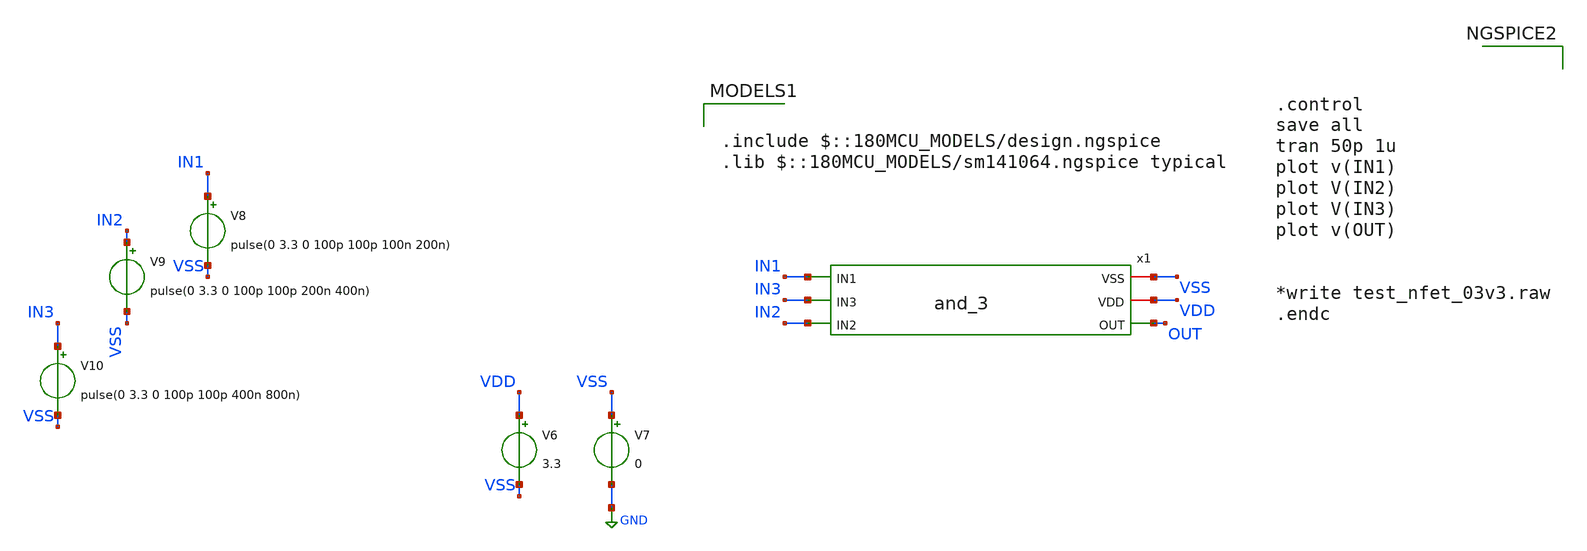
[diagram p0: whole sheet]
** sch_path: Clock_Generator_PAKISTAN_02/Schematics/and_3_TB_ibr.sch
**.subckt and_3_TB_ibr
V6 VDD VSS 3.3
V7 VSS GND 0
V8 IN1 VSS pulse(0 3.3 0 100p 100p 100n 200n)
V9 IN2 VSS pulse(0 3.3 0 100p 100p 200n 400n)
V10 IN3 VSS pulse(0 3.3 0 100p 100p 400n 800n)
x1 IN1 VSS VDD OUT IN3 IN2 and_3
**** begin user architecture code

.include $::180MCU_MODELS/design.ngspice
.lib $::180MCU_MODELS/sm141064.ngspice typical




.control
save all
tran 50p 1u
plot v(IN1)
plot V(IN2)
plot V(IN3)
plot v(OUT)


*write test_nfet_03v3.raw
.endc


**** end user architecture code
**.ends

* expanding   symbol:  and_3.sym # of pins=6
** sym_path: Clock_Generator_PAKISTAN_02/Schematics/and_3.sym
** sch_path: Clock_Generator_PAKISTAN_02/Schematics/and_3.sch
.subckt and_3 IN1 VSS VDD OUT IN3 IN2
*.ipin IN2
*.ipin IN1
*.iopin VSS
*.iopin VDD
*.opin OUT
*.ipin IN3
XM3 net2 IN3 VSS VSS nfet_03v3 L=0.28u W=0.22u nf=1 ad='int((nf+1)/2) * W/nf * 0.18u' as='int((nf+2)/2) * W/nf * 0.18u'
+ pd='2*int((nf+1)/2) * (W/nf + 0.18u)' ps='2*int((nf+2)/2) * (W/nf + 0.18u)' nrd='0.18u / W' nrs='0.18u / W'
+ sa=0 sb=0 sd=0 m=3
XM4 net1 IN1 net3 VSS nfet_03v3 L=0.28u W=0.22u nf=1 ad='int((nf+1)/2) * W/nf * 0.18u' as='int((nf+2)/2) * W/nf * 0.18u'
+ pd='2*int((nf+1)/2) * (W/nf + 0.18u)' ps='2*int((nf+2)/2) * (W/nf + 0.18u)' nrd='0.18u / W' nrs='0.18u / W'
+ sa=0 sb=0 sd=0 m=3
XM5 OUT net1 VSS VSS nfet_03v3 L=0.28u W=0.22u nf=1 ad='int((nf+1)/2) * W/nf * 0.18u' as='int((nf+2)/2) * W/nf * 0.18u'
+ pd='2*int((nf+1)/2) * (W/nf + 0.18u)' ps='2*int((nf+2)/2) * (W/nf + 0.18u)' nrd='0.18u / W' nrs='0.18u / W'
+ sa=0 sb=0 sd=0 m=1
XM6 OUT net1 VDD VDD pfet_03v3 L=0.28u W=0.8u nf=1 ad='int((nf+1)/2) * W/nf * 0.18u' as='int((nf+2)/2) * W/nf * 0.18u'
+ pd='2*int((nf+1)/2) * (W/nf + 0.18u)' ps='2*int((nf+2)/2) * (W/nf + 0.18u)' nrd='0.18u / W' nrs='0.18u / W'
+ sa=0 sb=0 sd=0 m=1
XM1 net1 IN3 VDD VDD pfet_03v3 L=0.28u W=0.8u nf=1 ad='int((nf+1)/2) * W/nf * 0.18u' as='int((nf+2)/2) * W/nf * 0.18u'
+ pd='2*int((nf+1)/2) * (W/nf + 0.18u)' ps='2*int((nf+2)/2) * (W/nf + 0.18u)' nrd='0.18u / W' nrs='0.18u / W'
+ sa=0 sb=0 sd=0 m=1
XM2 net1 IN1 VDD VDD pfet_03v3 L=0.28u W=0.8u nf=1 ad='int((nf+1)/2) * W/nf * 0.18u' as='int((nf+2)/2) * W/nf * 0.18u'
+ pd='2*int((nf+1)/2) * (W/nf + 0.18u)' ps='2*int((nf+2)/2) * (W/nf + 0.18u)' nrd='0.18u / W' nrs='0.18u / W'
+ sa=0 sb=0 sd=0 m=1
XM7 net3 IN2 net2 VSS nfet_03v3 L=0.28u W=0.22u nf=1 ad='int((nf+1)/2) * W/nf * 0.18u' as='int((nf+2)/2) * W/nf * 0.18u'
+ pd='2*int((nf+1)/2) * (W/nf + 0.18u)' ps='2*int((nf+2)/2) * (W/nf + 0.18u)' nrd='0.18u / W' nrs='0.18u / W'
+ sa=0 sb=0 sd=0 m=3
XM8 net1 IN2 VDD VDD pfet_03v3 L=0.28u W=0.8u nf=1 ad='int((nf+1)/2) * W/nf * 0.18u' as='int((nf+2)/2) * W/nf * 0.18u'
+ pd='2*int((nf+1)/2) * (W/nf + 0.18u)' ps='2*int((nf+2)/2) * (W/nf + 0.18u)' nrd='0.18u / W' nrs='0.18u / W'
+ sa=0 sb=0 sd=0 m=1
.ends

.GLOBAL GND
.end
